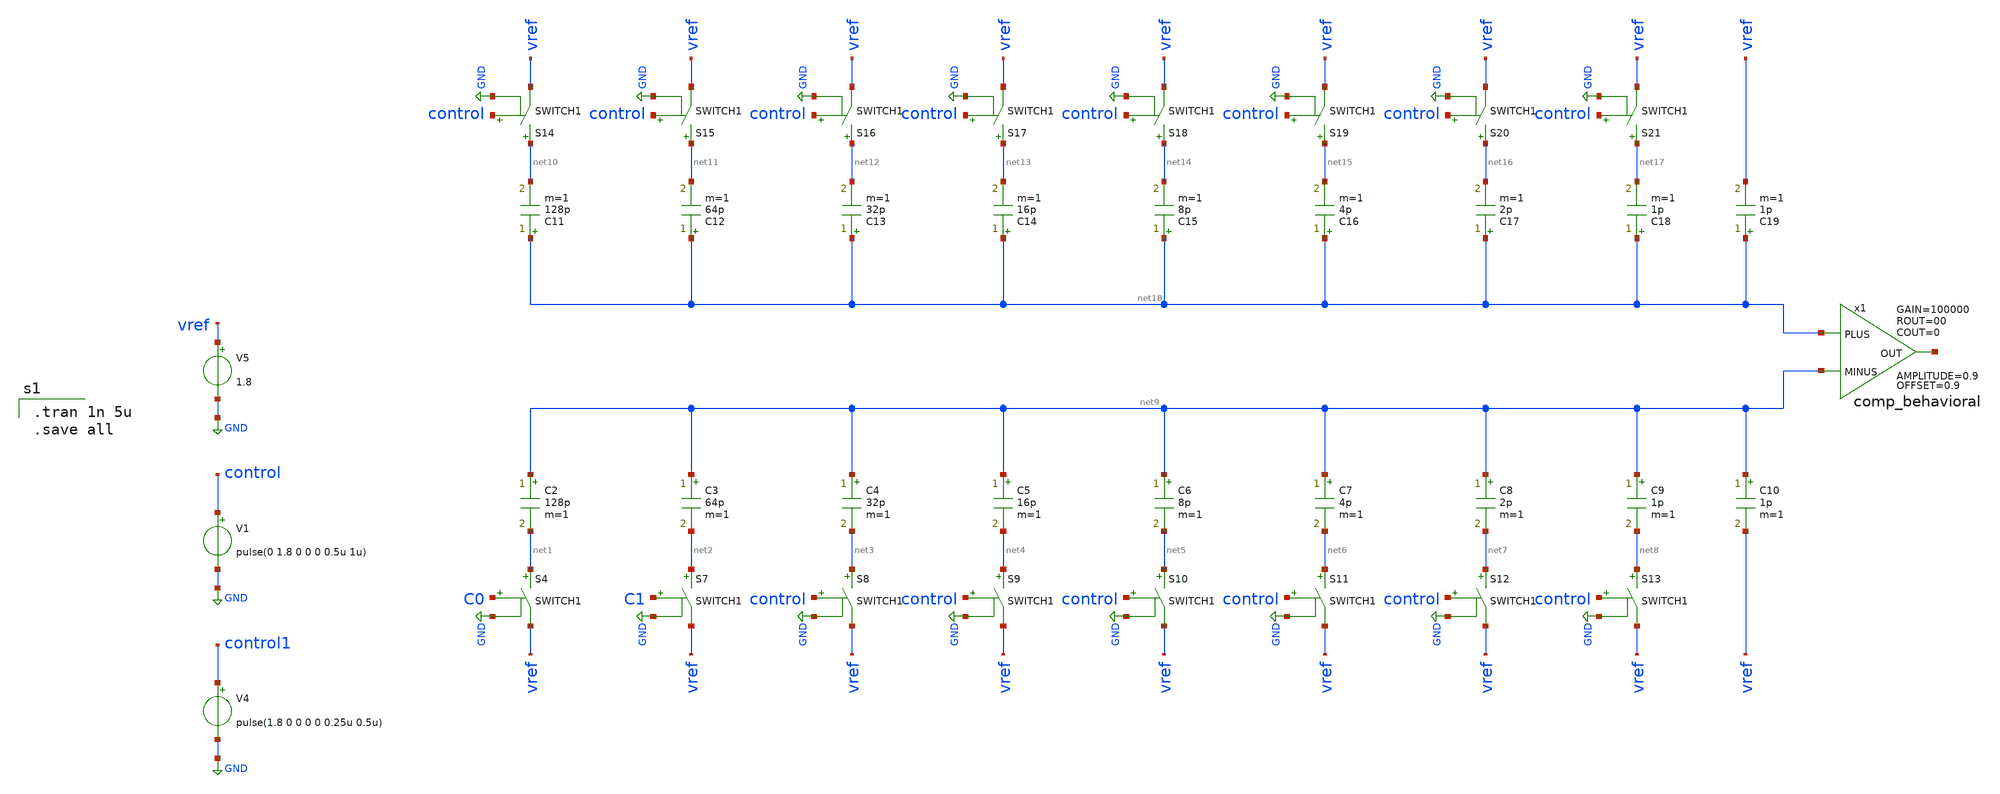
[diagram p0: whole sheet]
** sch_path: Behavioral_model/SAR_ADC_behavioral.sch
**.subckt SAR_ADC_behavioral
V1 control GND pulse(0 1.8 0 0 0 0.5u 1u)
V4 control1 GND pulse(1.8 0 0 0 0 0.25u 0.5u)
S4 net1 vref C0 GND SWITCH1
C2 net9 net1 128p m=1
V5 vref GND 1.8
S7 net2 vref C1 GND SWITCH1
C3 net9 net2 64p m=1
S8 net3 vref control GND SWITCH1
C4 net9 net3 32p m=1
S9 net4 vref control GND SWITCH1
C5 net9 net4 16p m=1
S10 net5 vref control GND SWITCH1
C6 net9 net5 8p m=1
S11 net6 vref control GND SWITCH1
C7 net9 net6 4p m=1
S12 net7 vref control GND SWITCH1
C8 net9 net7 2p m=1
S13 net8 vref control GND SWITCH1
C9 net9 net8 1p m=1
C10 net9 vref 1p m=1
S14 net10 vref control GND SWITCH1
C11 net18 net10 128p m=1
S15 net11 vref control GND SWITCH1
C12 net18 net11 64p m=1
S16 net12 vref control GND SWITCH1
C13 net18 net12 32p m=1
S17 net13 vref control GND SWITCH1
C14 net18 net13 16p m=1
S18 net14 vref control GND SWITCH1
C15 net18 net14 8p m=1
S19 net15 vref control GND SWITCH1
C16 net18 net15 4p m=1
S20 net16 vref control GND SWITCH1
C17 net18 net16 2p m=1
S21 net17 vref control GND SWITCH1
C18 net18 net17 1p m=1
C19 net18 vref 1p m=1
x1 net18 net9 net19 comp_behavioral OFFSET=0.9 AMPLITUDE=0.9 GAIN=100000 ROUT=00 COUT=0
**** begin user architecture code

.tran 1n 5u
.save all


.lib /usr/local/share/pdk/sky130A/libs.tech/ngspice/sky130.lib.spice tt


.model switch1 sw vt=0.1 vh=0 ron=1 roff=10G

**** end user architecture code
**.ends

* expanding   symbol:  comp_behavioral.sym # of pins=3
** sym_path: Behavioral_model/comp_behavioral.sym
** sch_path: Behavioral_model/comp_behavioral.sch
.subckt comp_behavioral PLUS MINUS OUT  OFFSET=0.9 AMPLITUDE=0.9 GAIN=100000 ROUT=00 COUT=0
*.ipin PLUS
*.ipin MINUS
*.opin OUT
B1 IOUT 0 V = {OFFSET + AMPLITUDE/2*(tanh(V(IPLUS,IMINUS)*GAIN*2/AMPLITUDE))}
V1 IPLUS PLUS 3
V2 IMINUS MINUS 3
R1 OUT IOUT {ROUT} m=1
C3 OUT 0 {COUT} m=1
.ends

.GLOBAL GND
.end
